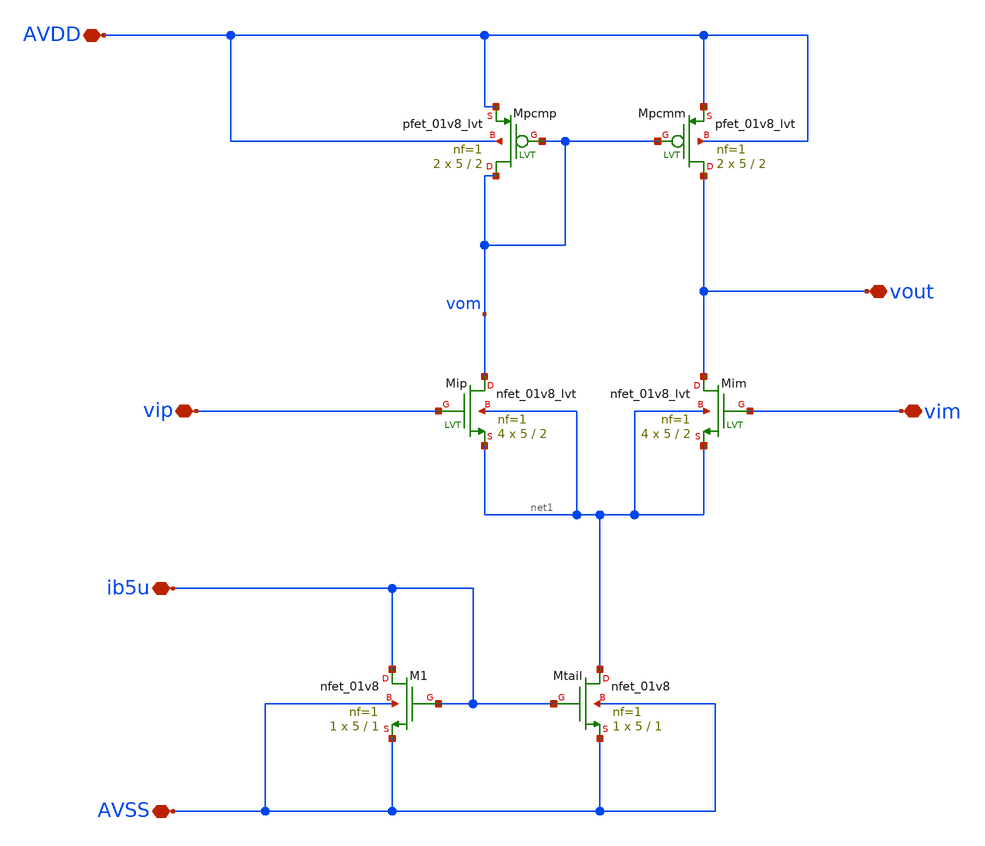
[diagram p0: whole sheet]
** sch_path: xschem/op_nmos.sch
**.subckt op_nmos ib5u AVSS vim vip AVDD vout
*.iopin ib5u
*.iopin AVSS
*.iopin vim
*.iopin vip
*.iopin AVDD
*.iopin vout
XM1 ib5u ib5u AVSS AVSS sky130_fd_pr__nfet_01v8 L=1 W=5 nf=1 ad='int((1 + 1)/2) * 5 / 1 * 0.29' as='int((1 + 2)/2) * 5 / 1 * 0.29'
+ pd='2*int((1 + 1)/2) * (5 / 1 + 0.29)' ps='2*int((1 + 2)/2) * (5 / 1 + 0.29)' nrd='0.29 / 5 ' nrs='0.29 / 5 '
+ sa=0 sb=0 sd=0 mult=1 m=1
XMtail net1 ib5u AVSS AVSS sky130_fd_pr__nfet_01v8 L=1 W=5 nf=1 ad='int((1 + 1)/2) * 5 / 1 * 0.29' as='int((1 + 2)/2) * 5 / 1 * 0.29'
+ pd='2*int((1 + 1)/2) * (5 / 1 + 0.29)' ps='2*int((1 + 2)/2) * (5 / 1 + 0.29)' nrd='0.29 / 5 ' nrs='0.29 / 5 '
+ sa=0 sb=0 sd=0 mult=1 m=1
XMip vom vip net1 net1 sky130_fd_pr__nfet_01v8_lvt L=2 W=5 nf=1 ad='int((1 + 1)/2) * 5 / 1 * 0.29' as='int((1 + 2)/2) * 5 / 1 * 0.29'
+ pd='2*int((1 + 1)/2) * (5 / 1 + 0.29)' ps='2*int((1 + 2)/2) * (5 / 1 + 0.29)' nrd='0.29 / 5 ' nrs='0.29 / 5 '
+ sa=0 sb=0 sd=0 mult=4 m=4
XMim vout vim net1 net1 sky130_fd_pr__nfet_01v8_lvt L=2 W=5 nf=1 ad='int((1 + 1)/2) * 5 / 1 * 0.29' as='int((1 + 2)/2) * 5 / 1 * 0.29'
+ pd='2*int((1 + 1)/2) * (5 / 1 + 0.29)' ps='2*int((1 + 2)/2) * (5 / 1 + 0.29)' nrd='0.29 / 5 ' nrs='0.29 / 5 '
+ sa=0 sb=0 sd=0 mult=4 m=4
XMpcmp vom vom AVDD AVDD sky130_fd_pr__pfet_01v8_lvt L=2 W=5 nf=1 ad='int((1 + 1)/2) * 5 / 1 * 0.29'
+ as='int((1 + 2)/2) * 5 / 1 * 0.29' pd='2*int((1 + 1)/2) * (5 / 1 + 0.29)' ps='2*int((1 + 2)/2) * (5 / 1 + 0.29)'
+ nrd='0.29 / 5 ' nrs='0.29 / 5 ' sa=0 sb=0 sd=0 mult=2 m=2
XMpcmm vout vom AVDD AVDD sky130_fd_pr__pfet_01v8_lvt L=2 W=5 nf=1 ad='int((1 + 1)/2) * 5 / 1 * 0.29'
+ as='int((1 + 2)/2) * 5 / 1 * 0.29' pd='2*int((1 + 1)/2) * (5 / 1 + 0.29)' ps='2*int((1 + 2)/2) * (5 / 1 + 0.29)'
+ nrd='0.29 / 5 ' nrs='0.29 / 5 ' sa=0 sb=0 sd=0 mult=2 m=2
**** begin user architecture code

** opencircuitdesign pdks install
.lib $::SKYWATER_MODELS/sky130.lib.spice tt

**** end user architecture code
**.ends
.end
